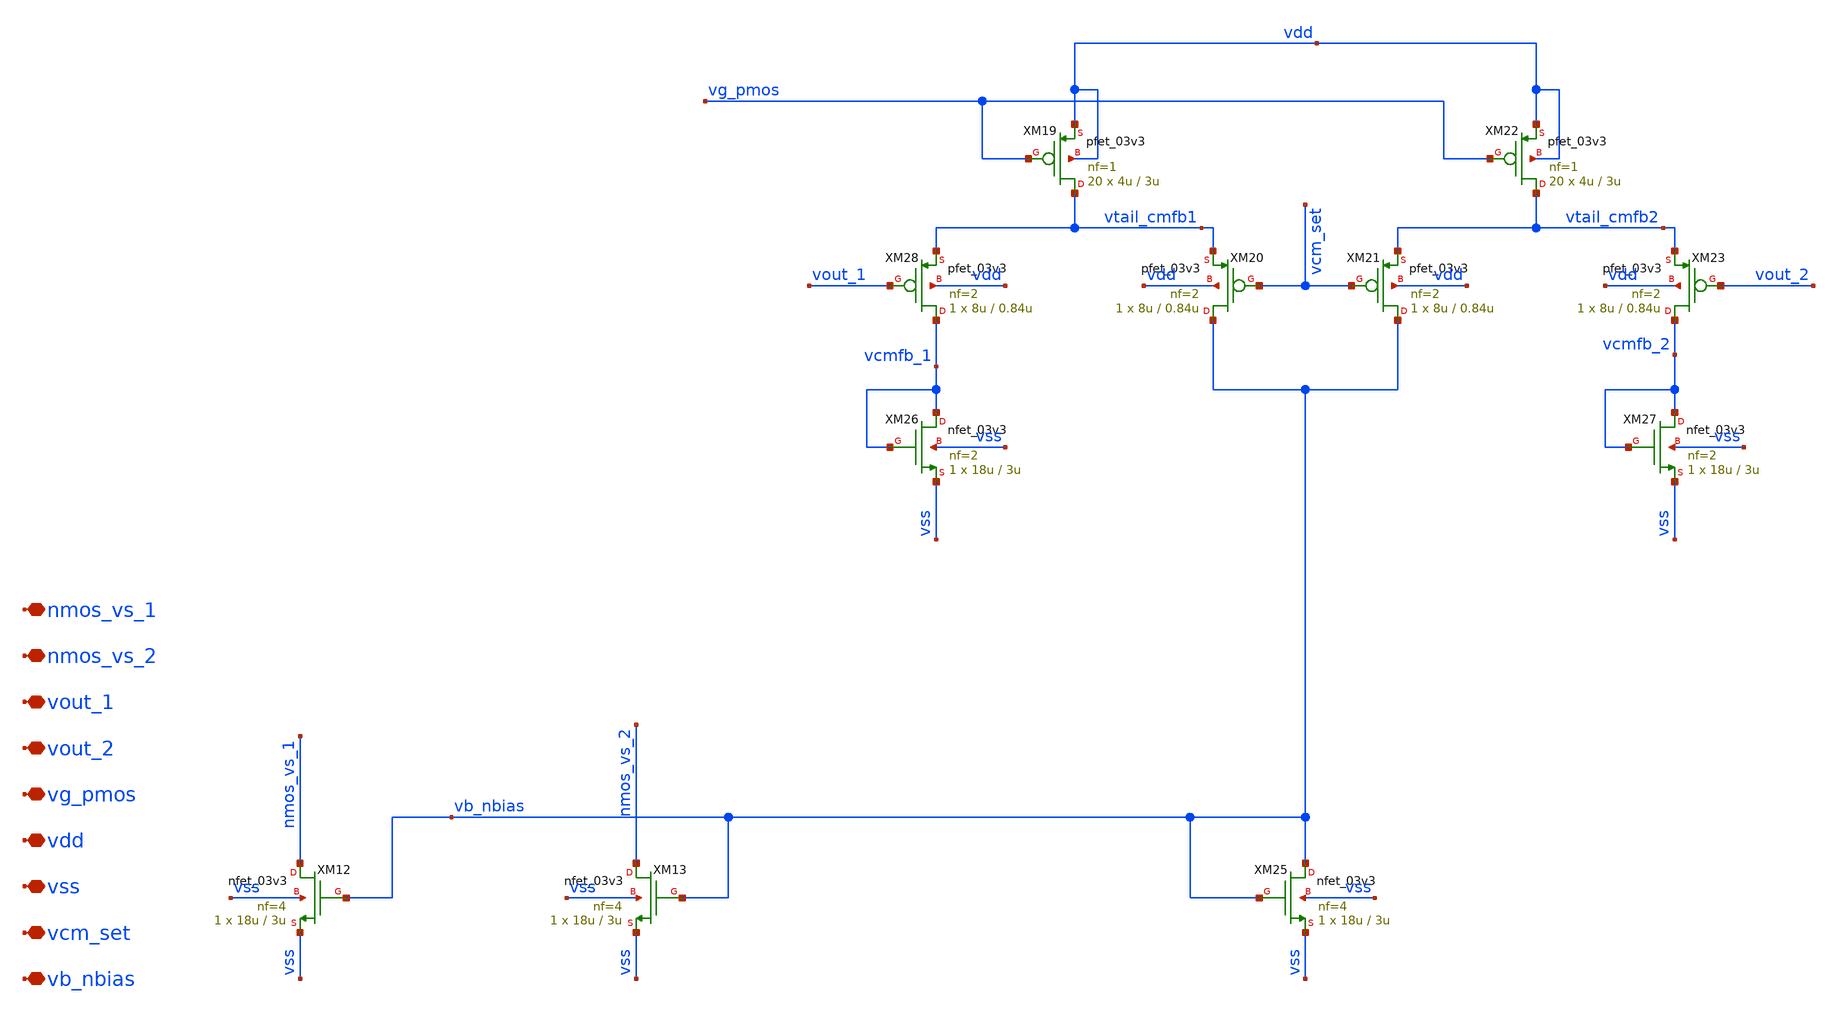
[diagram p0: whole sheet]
** sch_path: xschem/ccia_rrl_ota/b9_ccia_rrl_ota_cmfb.sch
**.subckt b9_ccia_rrl_ota_cmfb nmos_vs_1 nmos_vs_2 vout_1 vout_2 vg_pmos vdd vss vcm_set vb_nbias
*.iopin nmos_vs_1
*.iopin nmos_vs_2
*.iopin vout_1
*.iopin vout_2
*.iopin vg_pmos
*.iopin vdd
*.iopin vss
*.iopin vcm_set
*.iopin vb_nbias
XM12 nmos_vs_1 vb_nbias vss vss nfet_03v3 L=3u W=18u nf=4 ad='int((nf+1)/2) * W/nf * 0.18u' as='int((nf+2)/2) * W/nf * 0.18u'
+ pd='2*int((nf+1)/2) * (W/nf + 0.18u)' ps='2*int((nf+2)/2) * (W/nf + 0.18u)' nrd='0.18u / W' nrs='0.18u / W'
+ sa=0 sb=0 sd=0 m=1
XM13 nmos_vs_2 vb_nbias vss vss nfet_03v3 L=3u W=18u nf=4 ad='int((nf+1)/2) * W/nf * 0.18u' as='int((nf+2)/2) * W/nf * 0.18u'
+ pd='2*int((nf+1)/2) * (W/nf + 0.18u)' ps='2*int((nf+2)/2) * (W/nf + 0.18u)' nrd='0.18u / W' nrs='0.18u / W'
+ sa=0 sb=0 sd=0 m=1
XM19 vtail_cmfb1 vg_pmos vdd vdd pfet_03v3 L=3u W=4u nf=1 ad='int((nf+1)/2) * W/nf * 0.18u' as='int((nf+2)/2) * W/nf * 0.18u'
+ pd='2*int((nf+1)/2) * (W/nf + 0.18u)' ps='2*int((nf+2)/2) * (W/nf + 0.18u)' nrd='0.18u / W' nrs='0.18u / W'
+ sa=0 sb=0 sd=0 m=20
XM22 vtail_cmfb2 vg_pmos vdd vdd pfet_03v3 L=3u W=4u nf=1 ad='int((nf+1)/2) * W/nf * 0.18u' as='int((nf+2)/2) * W/nf * 0.18u'
+ pd='2*int((nf+1)/2) * (W/nf + 0.18u)' ps='2*int((nf+2)/2) * (W/nf + 0.18u)' nrd='0.18u / W' nrs='0.18u / W'
+ sa=0 sb=0 sd=0 m=20
XM25 vb_nbias vb_nbias vss vss nfet_03v3 L=3u W=18u nf=4 ad='int((nf+1)/2) * W/nf * 0.18u' as='int((nf+2)/2) * W/nf * 0.18u'
+ pd='2*int((nf+1)/2) * (W/nf + 0.18u)' ps='2*int((nf+2)/2) * (W/nf + 0.18u)' nrd='0.18u / W' nrs='0.18u / W'
+ sa=0 sb=0 sd=0 m=1
XM26 vcmfb_1 vcmfb_1 vss vss nfet_03v3 L=3u W=18u nf=2 ad='int((nf+1)/2) * W/nf * 0.18u' as='int((nf+2)/2) * W/nf * 0.18u'
+ pd='2*int((nf+1)/2) * (W/nf + 0.18u)' ps='2*int((nf+2)/2) * (W/nf + 0.18u)' nrd='0.18u / W' nrs='0.18u / W'
+ sa=0 sb=0 sd=0 m=1
XM27 vcmfb_2 vcmfb_2 vss vss nfet_03v3 L=3u W=18u nf=2 ad='int((nf+1)/2) * W/nf * 0.18u' as='int((nf+2)/2) * W/nf * 0.18u'
+ pd='2*int((nf+1)/2) * (W/nf + 0.18u)' ps='2*int((nf+2)/2) * (W/nf + 0.18u)' nrd='0.18u / W' nrs='0.18u / W'
+ sa=0 sb=0 sd=0 m=1
XM28 vcmfb_1 vout_1 vtail_cmfb1 vdd pfet_03v3 L=0.84u W=8u nf=2 ad='int((nf+1)/2) * W/nf * 0.18u' as='int((nf+2)/2) * W/nf * 0.18u'
+ pd='2*int((nf+1)/2) * (W/nf + 0.18u)' ps='2*int((nf+2)/2) * (W/nf + 0.18u)' nrd='0.18u / W' nrs='0.18u / W'
+ sa=0 sb=0 sd=0 m=1
XM20 vb_nbias vcm_set vtail_cmfb1 vdd pfet_03v3 L=0.84u W=8u nf=2 ad='int((nf+1)/2) * W/nf * 0.18u' as='int((nf+2)/2) * W/nf * 0.18u'
+ pd='2*int((nf+1)/2) * (W/nf + 0.18u)' ps='2*int((nf+2)/2) * (W/nf + 0.18u)' nrd='0.18u / W' nrs='0.18u / W'
+ sa=0 sb=0 sd=0 m=1
XM21 vb_nbias vcm_set vtail_cmfb2 vdd pfet_03v3 L=0.84u W=8u nf=2 ad='int((nf+1)/2) * W/nf * 0.18u' as='int((nf+2)/2) * W/nf * 0.18u'
+ pd='2*int((nf+1)/2) * (W/nf + 0.18u)' ps='2*int((nf+2)/2) * (W/nf + 0.18u)' nrd='0.18u / W' nrs='0.18u / W'
+ sa=0 sb=0 sd=0 m=1
XM23 vcmfb_2 vout_2 vtail_cmfb2 vdd pfet_03v3 L=0.84u W=8u nf=2 ad='int((nf+1)/2) * W/nf * 0.18u' as='int((nf+2)/2) * W/nf * 0.18u'
+ pd='2*int((nf+1)/2) * (W/nf + 0.18u)' ps='2*int((nf+2)/2) * (W/nf + 0.18u)' nrd='0.18u / W' nrs='0.18u / W'
+ sa=0 sb=0 sd=0 m=1
**.ends
.end
